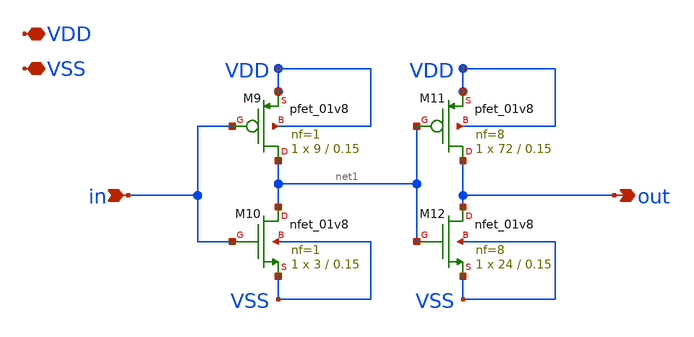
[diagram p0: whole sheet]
** sch_path: xschem/driver.sch
**.subckt driver VDD VSS out in
*.iopin VDD
*.iopin VSS
*.opin out
*.ipin in
XM9 net1 in VDD VDD sky130_fd_pr__pfet_01v8 L=0.15 W=9 nf=1 ad='int((nf+1)/2) * W/nf * 0.29' as='int((nf+2)/2) * W/nf * 0.29'
+ pd='2*int((nf+1)/2) * (W/nf + 0.29)' ps='2*int((nf+2)/2) * (W/nf + 0.29)' nrd='0.29 / W' nrs='0.29 / W'
+ sa=0 sb=0 sd=0 mult=1 m=1
XM10 net1 in VSS VSS sky130_fd_pr__nfet_01v8 L=0.15 W=3 nf=1 ad='int((nf+1)/2) * W/nf * 0.29' as='int((nf+2)/2) * W/nf * 0.29'
+ pd='2*int((nf+1)/2) * (W/nf + 0.29)' ps='2*int((nf+2)/2) * (W/nf + 0.29)' nrd='0.29 / W' nrs='0.29 / W'
+ sa=0 sb=0 sd=0 mult=1 m=1
XM11 out net1 VDD VDD sky130_fd_pr__pfet_01v8 L=0.15 W=72 nf=8 ad='int((nf+1)/2) * W/nf * 0.29' as='int((nf+2)/2) * W/nf * 0.29'
+ pd='2*int((nf+1)/2) * (W/nf + 0.29)' ps='2*int((nf+2)/2) * (W/nf + 0.29)' nrd='0.29 / W' nrs='0.29 / W'
+ sa=0 sb=0 sd=0 mult=1 m=1
XM12 out net1 VSS VSS sky130_fd_pr__nfet_01v8 L=0.15 W=24 nf=8 ad='int((nf+1)/2) * W/nf * 0.29' as='int((nf+2)/2) * W/nf * 0.29'
+ pd='2*int((nf+1)/2) * (W/nf + 0.29)' ps='2*int((nf+2)/2) * (W/nf + 0.29)' nrd='0.29 / W' nrs='0.29 / W'
+ sa=0 sb=0 sd=0 mult=1 m=1
**.ends
.end
